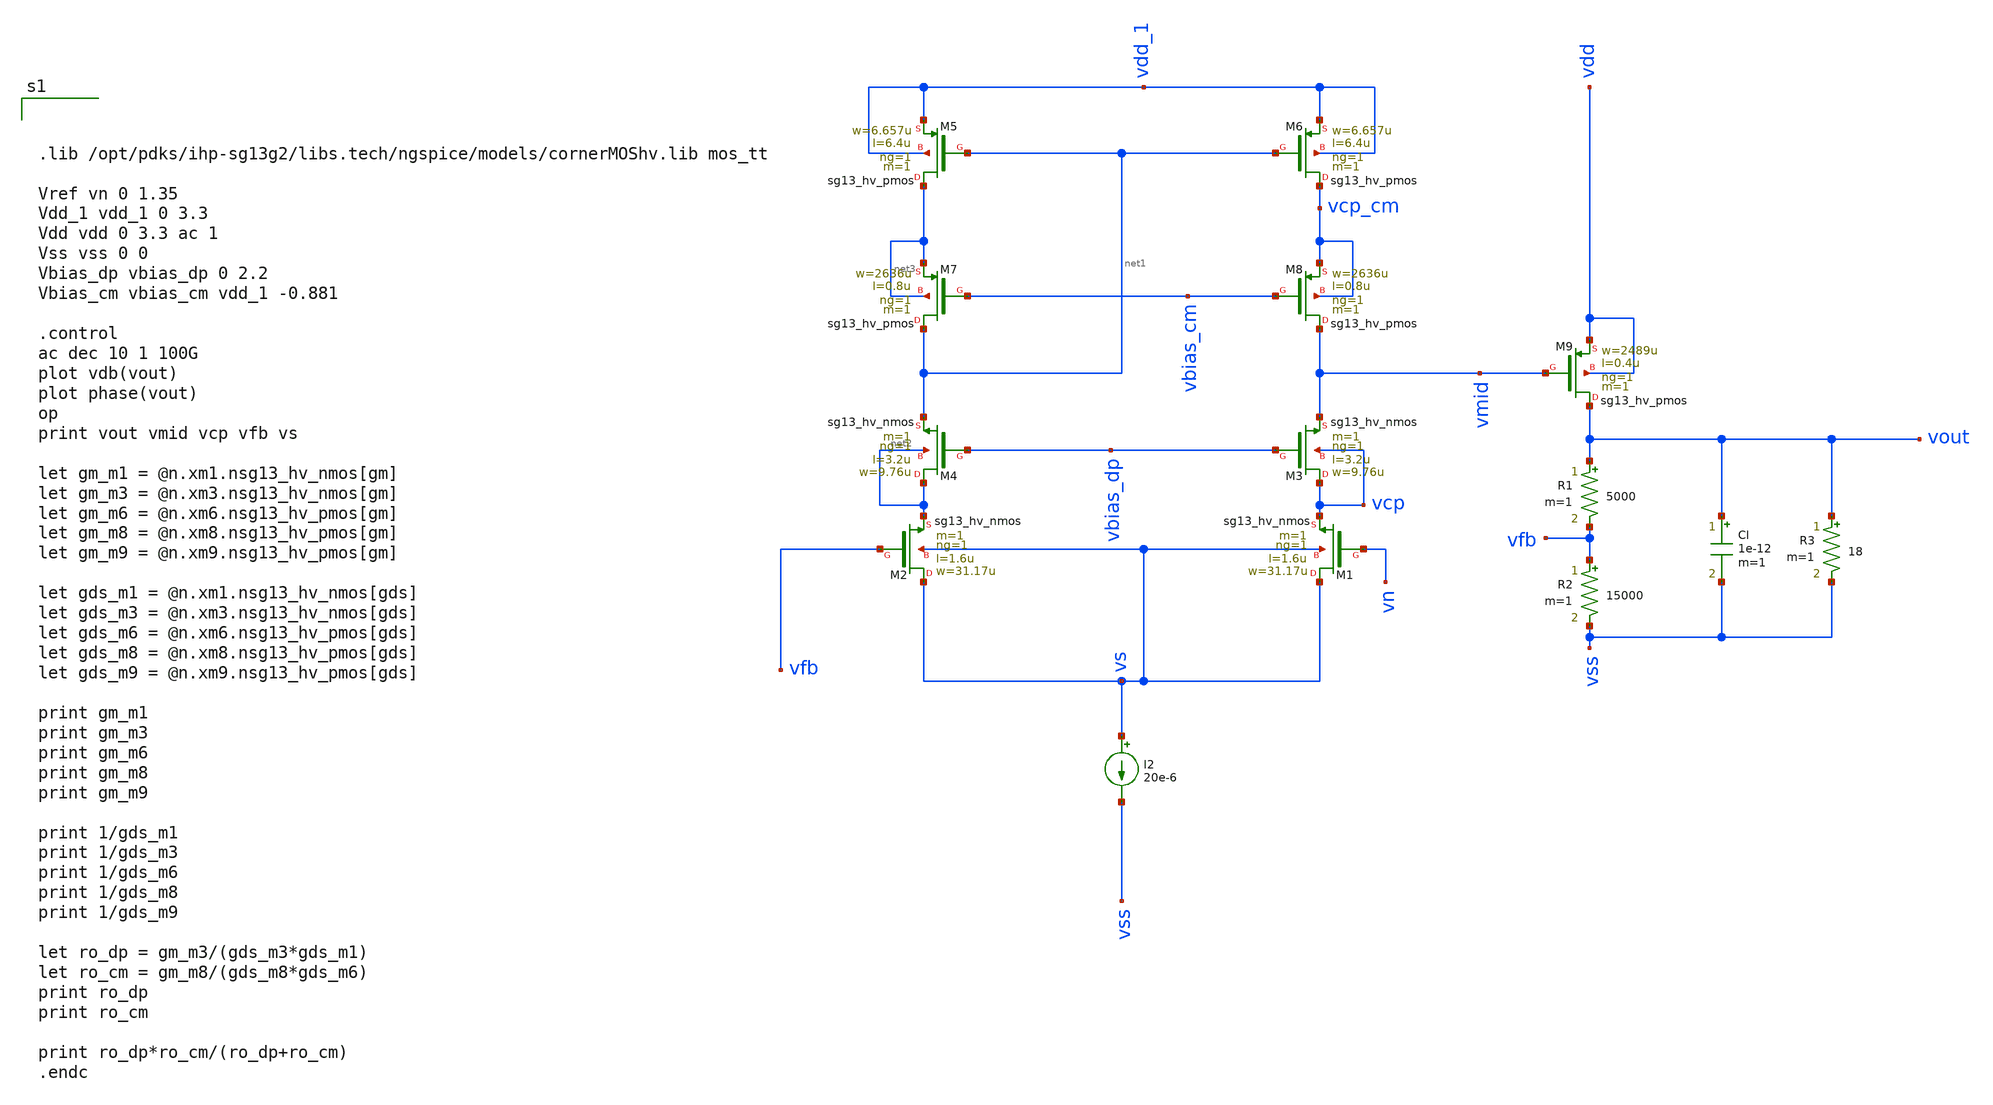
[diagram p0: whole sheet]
** sch_path: test-python/Tesis_notebooks/xschem/ldo_sim_ihp_cc_full.sch
**.subckt ldo_sim_ihp_cc_full
R1 vout vfb 5000 m=1
R2 vfb vss 15000 m=1
Cl vout vss 1e-12 m=1
XM7 net1 vbias_cm net3 net3 sg13_hv_pmos w=2636u l=0.8u ng=1 m=1 mm_ok=1
I2 vs vss 20e-6
XM1 vs vn vcp vs sg13_hv_nmos w=31.17u l=1.6u ng=1 m=1 mm_ok=1
XM2 vs vfb net2 vs sg13_hv_nmos w=31.17u l=1.6u ng=1 m=1 mm_ok=1
XM3 vcp vbias_dp vmid vcp sg13_hv_nmos w=9.76u l=3.2u ng=1 m=1 mm_ok=1
XM4 net2 vbias_dp net1 net2 sg13_hv_nmos w=9.76u l=3.2u ng=1 m=1 mm_ok=1
XM5 net3 net1 vdd_1 vdd_1 sg13_hv_pmos w=6.657u l=6.4u ng=1 m=1 mm_ok=1
XM6 vcp_cm net1 vdd_1 vdd_1 sg13_hv_pmos w=6.657u l=6.4u ng=1 m=1 mm_ok=1
XM8 vmid vbias_cm vcp_cm vcp_cm sg13_hv_pmos w=2636u l=0.8u ng=1 m=1 mm_ok=1
XM9 vout vmid vdd vdd sg13_hv_pmos w=2489u l=0.4u ng=1 m=1 mm_ok=1
R3 vout vss 18 m=1
**** begin user architecture code



.lib /opt/pdks/ihp-sg13g2/libs.tech/ngspice/models/cornerMOShv.lib mos_tt

Vref vn 0 1.35
Vdd_1 vdd_1 0 3.3
Vdd vdd 0 3.3 ac 1
Vss vss 0 0
Vbias_dp vbias_dp 0 2.2
Vbias_cm vbias_cm vdd_1 -0.881

.control
ac dec 10 1 100G
plot vdb(vout)
plot phase(vout)
op
print vout vmid vcp vfb vs

let gm_m1 = @n.xm1.nsg13_hv_nmos[gm]
let gm_m3 = @n.xm3.nsg13_hv_nmos[gm]
let gm_m6 = @n.xm6.nsg13_hv_pmos[gm]
let gm_m8 = @n.xm8.nsg13_hv_pmos[gm]
let gm_m9 = @n.xm9.nsg13_hv_pmos[gm]

let gds_m1 = @n.xm1.nsg13_hv_nmos[gds]
let gds_m3 = @n.xm3.nsg13_hv_nmos[gds]
let gds_m6 = @n.xm6.nsg13_hv_pmos[gds]
let gds_m8 = @n.xm8.nsg13_hv_pmos[gds]
let gds_m9 = @n.xm9.nsg13_hv_pmos[gds]

print gm_m1
print gm_m3
print gm_m6
print gm_m8
print gm_m9

print 1/gds_m1
print 1/gds_m3
print 1/gds_m6
print 1/gds_m8
print 1/gds_m9

let ro_dp = gm_m3/(gds_m3*gds_m1)
let ro_cm = gm_m8/(gds_m8*gds_m6)
print ro_dp
print ro_cm

print ro_dp*ro_cm/(ro_dp+ro_cm)
.endc



**** end user architecture code
**.ends
.end
